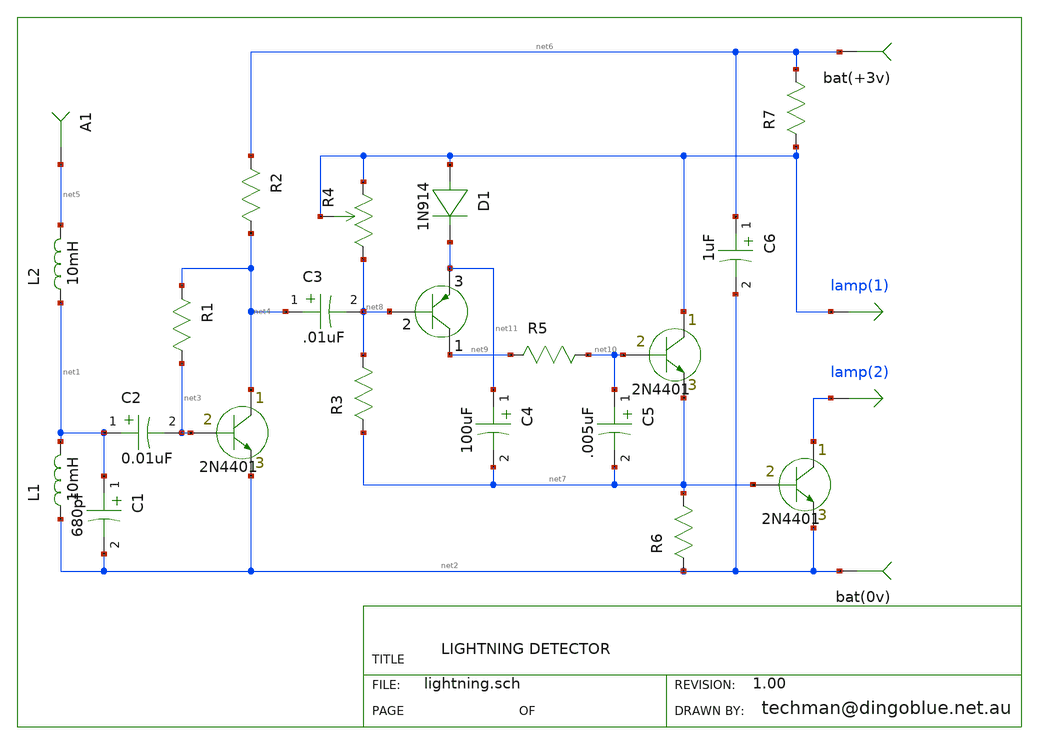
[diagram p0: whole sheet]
** sch_path: xschem_library/gschem_import/lightning.sch
**.subckt lightning lamp(1) lamp(2)
L1 net2 net1 10mH
L2 net1 net5 10mH
C2 net1 net3 0.01uF
C1 net1 net2 680pf
C3 net4 net8 .01uF
C4 net11 net7 100uF
C5 net10 net7 .005uF
R1 net3 net4 180k
R2 net4 net6 3.9k
R7 net6 lamp(1) 47R
R3 net8 net7 22k
R5 net10 net9 2.2K
R6 net7 net2 2.7k
R4 net8 lamp(1) lamp(1) 20k
bat(+3v) net6
bat(0v) net2
A1 net5
C6 net6 net2 1uF
D1 lamp(1) net11 1N914
Q1 net4 net3 net2 2N4401
Q2 net9 net11 net8 2N4403
Q3 lamp(1) net10 net7 2N4401
Q4 lamp(2) net7 net2 2N4401
**.ends
.end
